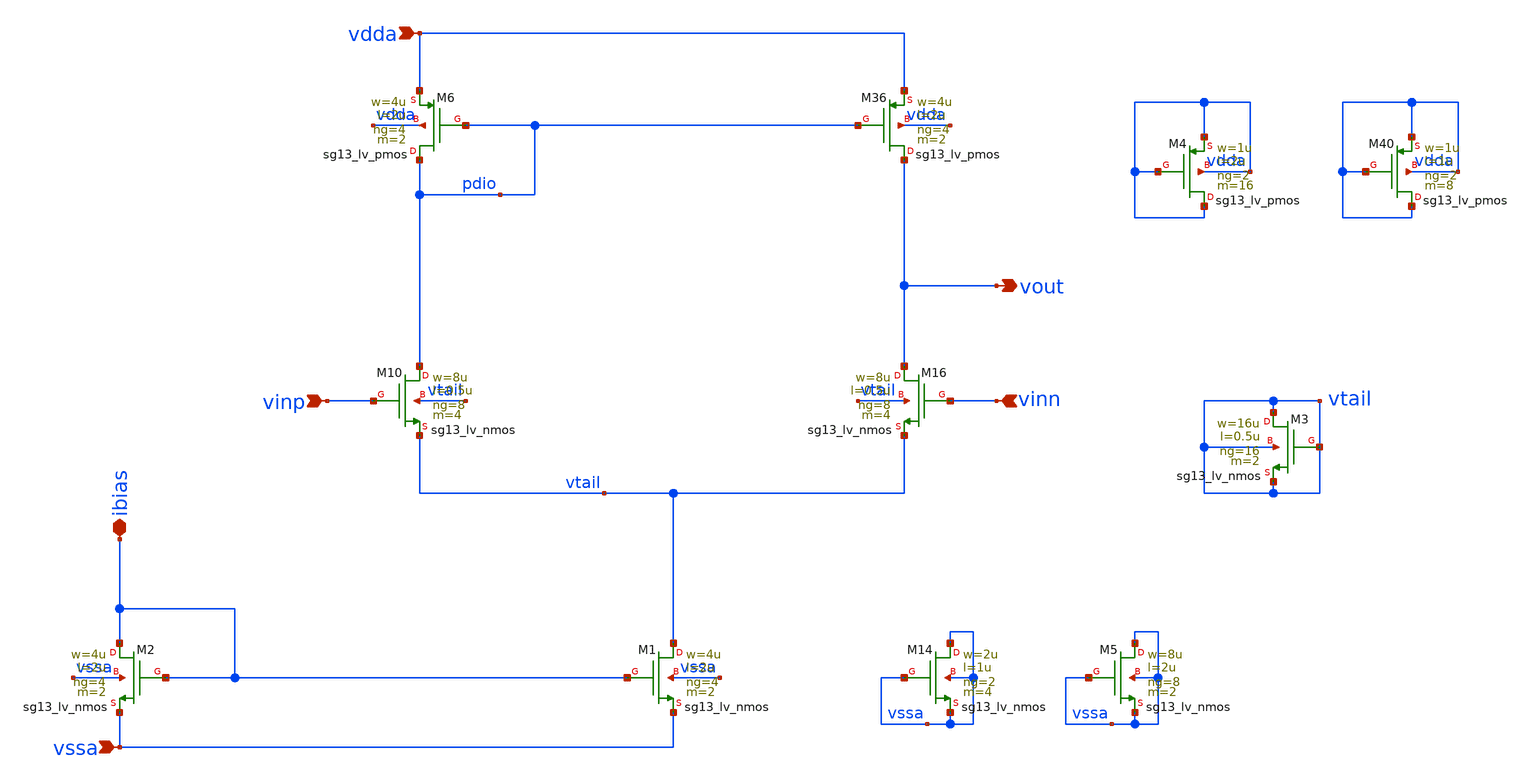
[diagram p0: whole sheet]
** sch_path: tb_OTA_1stage_ihp/OTA_bu.sch
**.subckt OTA_bu ibias vdda vssa vinp vinn vout
*.iopin ibias
*.ipin vdda
*.ipin vssa
*.ipin vinp
*.ipin vinn
*.opin vout
XM6 pdio pdio vdda vdda sg13_lv_pmos w=4u l=2u ng=4 m=2 mm_ok=1
XM1 vtail ibias vssa vssa sg13_lv_nmos w=4u l=2u ng=4 m=2 mm_ok=1
XM2 ibias ibias vssa vssa sg13_lv_nmos w=4u l=2u ng=4 m=2 mm_ok=1
XM3 vtail vtail vtail vtail sg13_lv_nmos w=16u l=0.5u ng=16 m=2 mm_ok=1
XM10 pdio vinp vtail vtail sg13_lv_nmos w=8u l=0.5u ng=8 m=4 mm_ok=1
XM14 vssa vssa vssa vssa sg13_lv_nmos w=2u l=1u ng=2 m=4 mm_ok=1
XM16 vout vinn vtail vtail sg13_lv_nmos w=8u l=0.5u ng=8 m=4 mm_ok=1
XM36 vout pdio vdda vdda sg13_lv_pmos w=4u l=2u ng=4 m=2 mm_ok=1
XM40 vdda vdda vdda vdda sg13_lv_pmos w=1u l=1u ng=2 m=8 mm_ok=1
XM4 vdda vdda vdda vdda sg13_lv_pmos w=1u l=2u ng=2 m=16 mm_ok=1
XM5 vssa vssa vssa vssa sg13_lv_nmos w=8u l=2u ng=8 m=2 mm_ok=1
**.ends
.end
